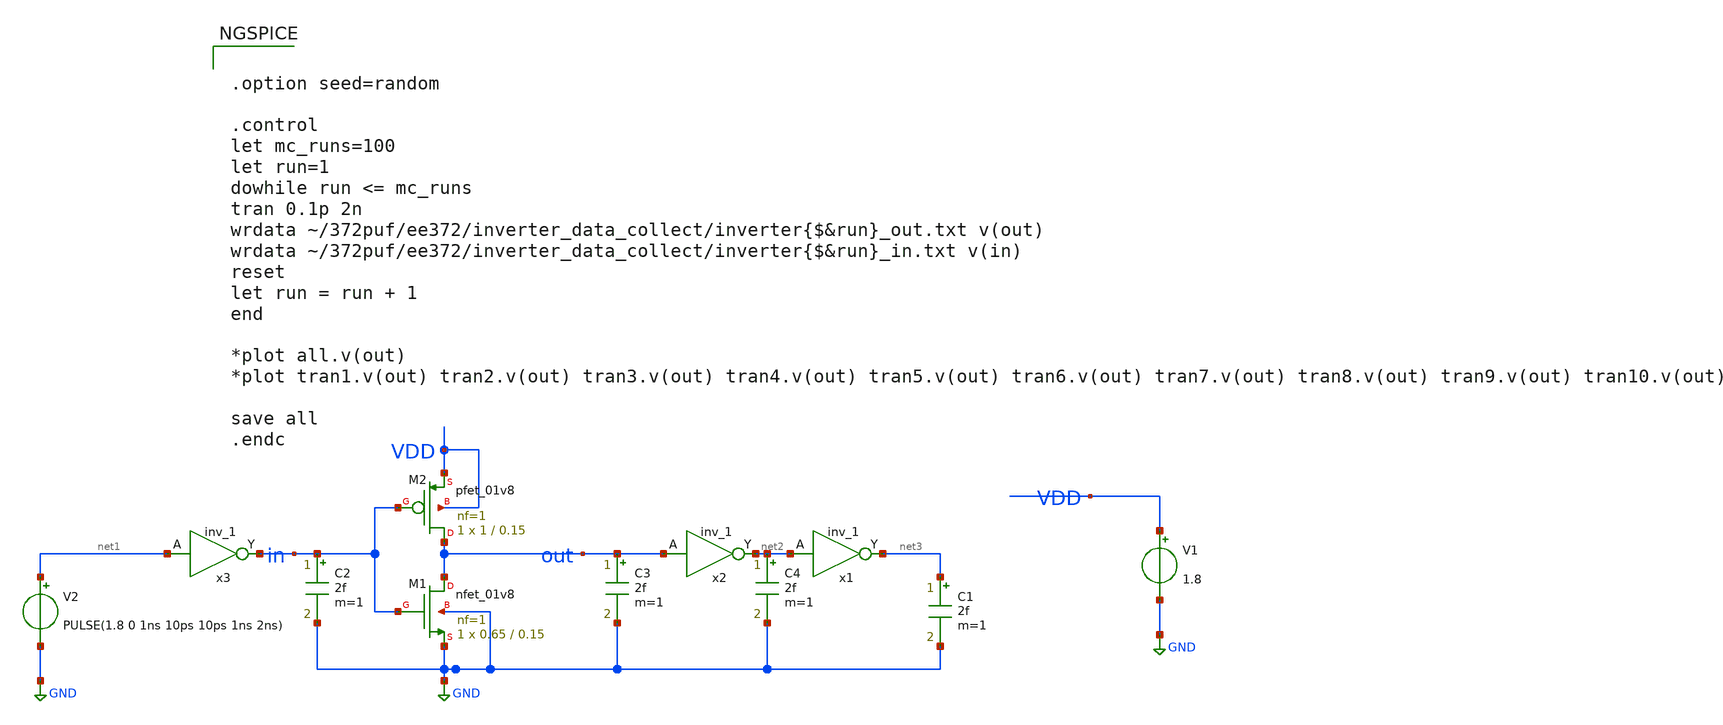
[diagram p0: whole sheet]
** sch_path: xiaolin/inv_testrise.sch
**.subckt inv_testrise
V1 VDD GND 1.8
V2 net1 GND PULSE(1.8 0 1ns 10ps 10ps 1ns 2ns)
x1 net2 GND GND VDD VDD net3 sky130_fd_sc_hd__inv_1
x2 out GND GND VDD VDD net2 sky130_fd_sc_hd__inv_1
XM1 out in GND GND sky130_fd_pr__nfet_01v8 L=0.15 W=0.65 nf=1 ad='int((nf+1)/2) * W/nf * 0.29' as='int((nf+2)/2) * W/nf * 0.29'
+ pd='2*int((nf+1)/2) * (W/nf + 0.29)' ps='2*int((nf+2)/2) * (W/nf + 0.29)' nrd='0.29 / W' nrs='0.29 / W'
+ sa=0 sb=0 sd=0 mult=1 m=1
XM2 out in VDD VDD sky130_fd_pr__pfet_01v8 L=0.15 W=1 nf=1 ad='int((nf+1)/2) * W/nf * 0.29' as='int((nf+2)/2) * W/nf * 0.29'
+ pd='2*int((nf+1)/2) * (W/nf + 0.29)' ps='2*int((nf+2)/2) * (W/nf + 0.29)' nrd='0.29 / W' nrs='0.29 / W'
+ sa=0 sb=0 sd=0 mult=1 m=1
C1 net3 GND 2f m=1
x3 net1 GND GND VDD VDD in sky130_fd_sc_hd__inv_1
C2 in GND 2f m=1
C3 out GND 2f m=1
C4 net2 GND 2f m=1
**** begin user architecture code


.lib /farmshare/home/classes/ee/372/PDKs/open_pdks_1.0.310/sky130/sky130A/libs.tech/ngspice/sky130.lib.spice tt_mm
.include /farmshare/home/classes/ee/372/PDKs/open_pdks_1.0.310/sky130/sky130A/libs.ref/sky130_fd_sc_hd/spice/sky130_fd_sc_hd.spice




.option seed=random

.control
let mc_runs=100
let run=1
dowhile run <= mc_runs
tran 0.1p 2n
wrdata ~/372puf/ee372/inverter_data_collect/inverter{$&run}_out.txt v(out)
wrdata ~/372puf/ee372/inverter_data_collect/inverter{$&run}_in.txt v(in)
reset
let run = run + 1
end

*plot all.v(out)
*plot tran1.v(out) tran2.v(out) tran3.v(out) tran4.v(out) tran5.v(out) tran6.v(out) tran7.v(out)
*+ tran8.v(out) tran9.v(out) tran10.v(out)

save all
.endc


**** end user architecture code
**.ends
.GLOBAL GND
.end
